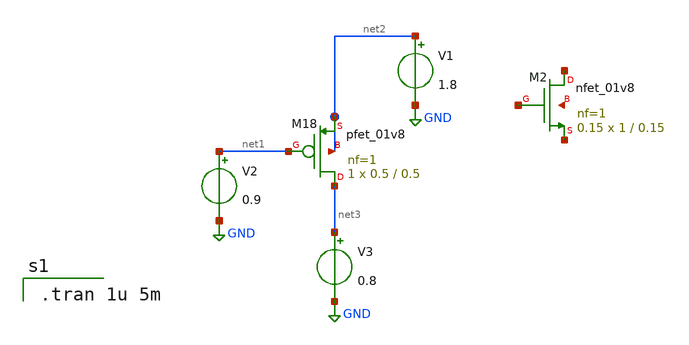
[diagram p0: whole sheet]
** sch_path: xschem/xschemfiles/nfet_test.sch
**.subckt nfet_test
XM2 net4 net5 net6 net7 sky130_fd_pr__nfet_01v8 L=0.15 W=1 nf=1 ad='int((1 + 1)/2) * 1 / 1 * 0.29' as='int((1 + 2)/2) * 1 / 1 * 0.29'
+ pd='2*int((1 + 1)/2) * (1 / 1 + 0.29)' ps='2*int((1 + 2)/2) * (1 / 1 + 0.29)' nrd='0.29 / 1 ' nrs='0.29 / 1 '
+ sa=0 sb=0 sd=0 mult=0.15 m=0.15
V1 net2 GND 1.8
V2 net1 GND 0.9
XM18 net3 net1 net2 net2 sky130_fd_pr__pfet_01v8 L=0.5 W=0.5 nf=1 ad='int((nf+1)/2) * W/nf * 0.29' as='int((nf+2)/2) * W/nf * 0.29'
+ pd='2*int((nf+1)/2) * (W/nf + 0.29)' ps='2*int((nf+2)/2) * (W/nf + 0.29)' nrd='0.29 / W' nrs='0.29 / W'
+ sa=0 sb=0 sd=0 mult=1 m=1
V3 net3 GND 0.8
**** begin user architecture code

** opencircuitdesign pdks install
.lib $::SKYWATER_MODELS/sky130.lib.spice tt



.tran 1u 5m

**** end user architecture code
**.ends
.GLOBAL GND
.end
